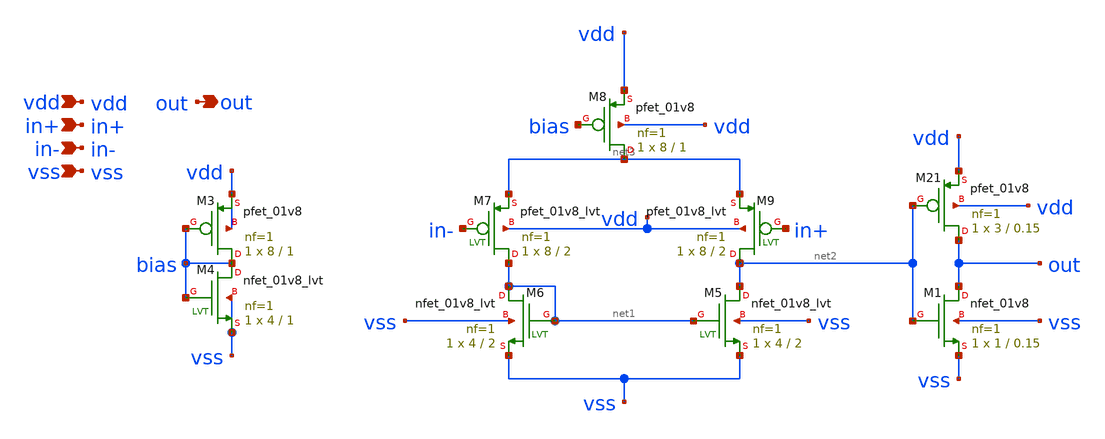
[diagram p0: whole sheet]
** sch_path: custom_gds/tt_um_tim2305_adc_dac/xschem/compr.sch
**.subckt compr in+ in- vdd out vss
*.ipin in+
*.ipin in-
*.ipin vdd
*.opin out
*.ipin vss
XM3 bias bias vdd vdd sky130_fd_pr__pfet_01v8 L=1 W=8 nf=1 ad='int((nf+1)/2) * W/nf * 0.29' as='int((nf+2)/2) * W/nf * 0.29'
+ pd='2*int((nf+1)/2) * (W/nf + 0.29)' ps='2*int((nf+2)/2) * (W/nf + 0.29)' nrd='0.29 / W' nrs='0.29 / W'
+ sa=0 sb=0 sd=0 mult=1 m=1
XM8 net3 bias vdd vdd sky130_fd_pr__pfet_01v8 L=1 W=8 nf=1 ad='int((nf+1)/2) * W/nf * 0.29' as='int((nf+2)/2) * W/nf * 0.29'
+ pd='2*int((nf+1)/2) * (W/nf + 0.29)' ps='2*int((nf+2)/2) * (W/nf + 0.29)' nrd='0.29 / W' nrs='0.29 / W'
+ sa=0 sb=0 sd=0 mult=1 m=1
XM5 net2 net1 vss vss sky130_fd_pr__nfet_01v8_lvt L=2 W=4 nf=1 ad='int((nf+1)/2) * W/nf * 0.29' as='int((nf+2)/2) * W/nf * 0.29'
+ pd='2*int((nf+1)/2) * (W/nf + 0.29)' ps='2*int((nf+2)/2) * (W/nf + 0.29)' nrd='0.29 / W' nrs='0.29 / W'
+ sa=0 sb=0 sd=0 mult=1 m=1
XM6 net1 net1 vss vss sky130_fd_pr__nfet_01v8_lvt L=2 W=4 nf=1 ad='int((nf+1)/2) * W/nf * 0.29' as='int((nf+2)/2) * W/nf * 0.29'
+ pd='2*int((nf+1)/2) * (W/nf + 0.29)' ps='2*int((nf+2)/2) * (W/nf + 0.29)' nrd='0.29 / W' nrs='0.29 / W'
+ sa=0 sb=0 sd=0 mult=1 m=1
XM7 net1 in- net3 vdd sky130_fd_pr__pfet_01v8_lvt L=2 W=8 nf=1 ad='int((nf+1)/2) * W/nf * 0.29' as='int((nf+2)/2) * W/nf * 0.29'
+ pd='2*int((nf+1)/2) * (W/nf + 0.29)' ps='2*int((nf+2)/2) * (W/nf + 0.29)' nrd='0.29 / W' nrs='0.29 / W'
+ sa=0 sb=0 sd=0 mult=1 m=1
XM9 net2 in+ net3 vdd sky130_fd_pr__pfet_01v8_lvt L=2 W=8 nf=1 ad='int((nf+1)/2) * W/nf * 0.29' as='int((nf+2)/2) * W/nf * 0.29'
+ pd='2*int((nf+1)/2) * (W/nf + 0.29)' ps='2*int((nf+2)/2) * (W/nf + 0.29)' nrd='0.29 / W' nrs='0.29 / W'
+ sa=0 sb=0 sd=0 mult=1 m=1
XM4 bias bias vss vss sky130_fd_pr__nfet_01v8_lvt L=1 W=4 nf=1 ad='int((nf+1)/2) * W/nf * 0.29' as='int((nf+2)/2) * W/nf * 0.29'
+ pd='2*int((nf+1)/2) * (W/nf + 0.29)' ps='2*int((nf+2)/2) * (W/nf + 0.29)' nrd='0.29 / W' nrs='0.29 / W'
+ sa=0 sb=0 sd=0 mult=1 m=1
XM21 out net2 vdd vdd sky130_fd_pr__pfet_01v8 L=0.15 W=3 nf=1 ad='int((nf+1)/2) * W/nf * 0.29' as='int((nf+2)/2) * W/nf * 0.29'
+ pd='2*int((nf+1)/2) * (W/nf + 0.29)' ps='2*int((nf+2)/2) * (W/nf + 0.29)' nrd='0.29 / W' nrs='0.29 / W'
+ sa=0 sb=0 sd=0 mult=1 m=1
XM1 out net2 vss vss sky130_fd_pr__nfet_01v8 L=0.15 W=1 nf=1 ad='int((nf+1)/2) * W/nf * 0.29' as='int((nf+2)/2) * W/nf * 0.29'
+ pd='2*int((nf+1)/2) * (W/nf + 0.29)' ps='2*int((nf+2)/2) * (W/nf + 0.29)' nrd='0.29 / W' nrs='0.29 / W'
+ sa=0 sb=0 sd=0 mult=1 m=1
**.ends
.end
